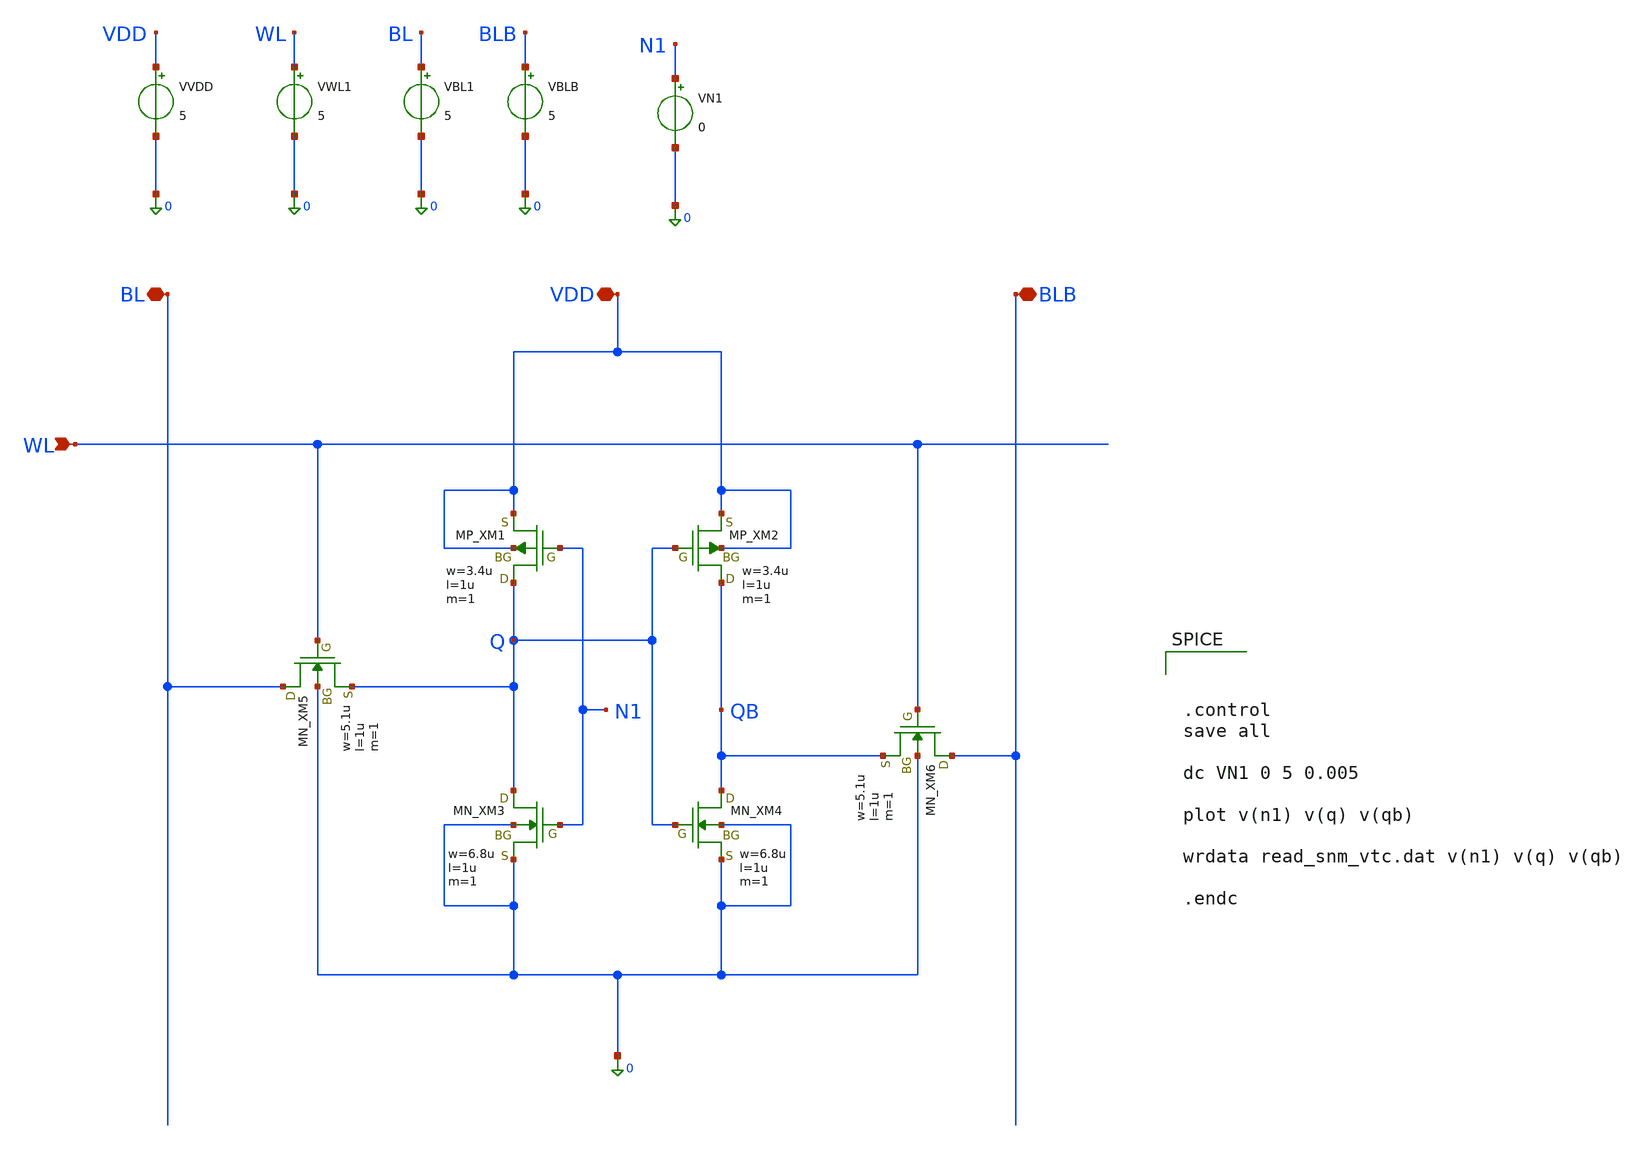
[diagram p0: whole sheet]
** sch_path: cell/snm/tb_read_snm.sch
**.subckt tb_read_snm BL BLB WL VDD
*.iopin BL
*.iopin BLB
*.ipin WL
*.iopin VDD
XXM1 Q N1 VDD VDD PMOS w=3.4u l=1u nrd=0 nrs=0 m=1
XXM2 QB Q VDD VDD PMOS w=3.4u l=1u nrd=0 nrs=0 m=1
XXM4 QB Q 0 0 NMOS w=6.8u l=1u nrd=0 nrs=0 m=1
XXM3 Q N1 0 0 NMOS w=6.8u l=1u nrd=0 nrs=0 m=1
XXM5 BL WL Q 0 NMOS w=5.1u l=1u nrd=0 nrs=0 m=1
XXM6 BLB WL QB 0 NMOS w=5.1u l=1u nrd=0 nrs=0 m=1
VVDD VDD 0 5
VWL1 WL 0 5
VBLB BLB 0 5
VBL1 BL 0 5
VN1 N1 0 0
**** begin user architecture code
 .include $::LIB/ip62_models



.control
save all

dc VN1 0 5 0.005

plot v(n1) v(q) v(qb)

wrdata read_snm_vtc.dat v(n1) v(q) v(qb)

.endc


**** end user architecture code
**.ends
.end
